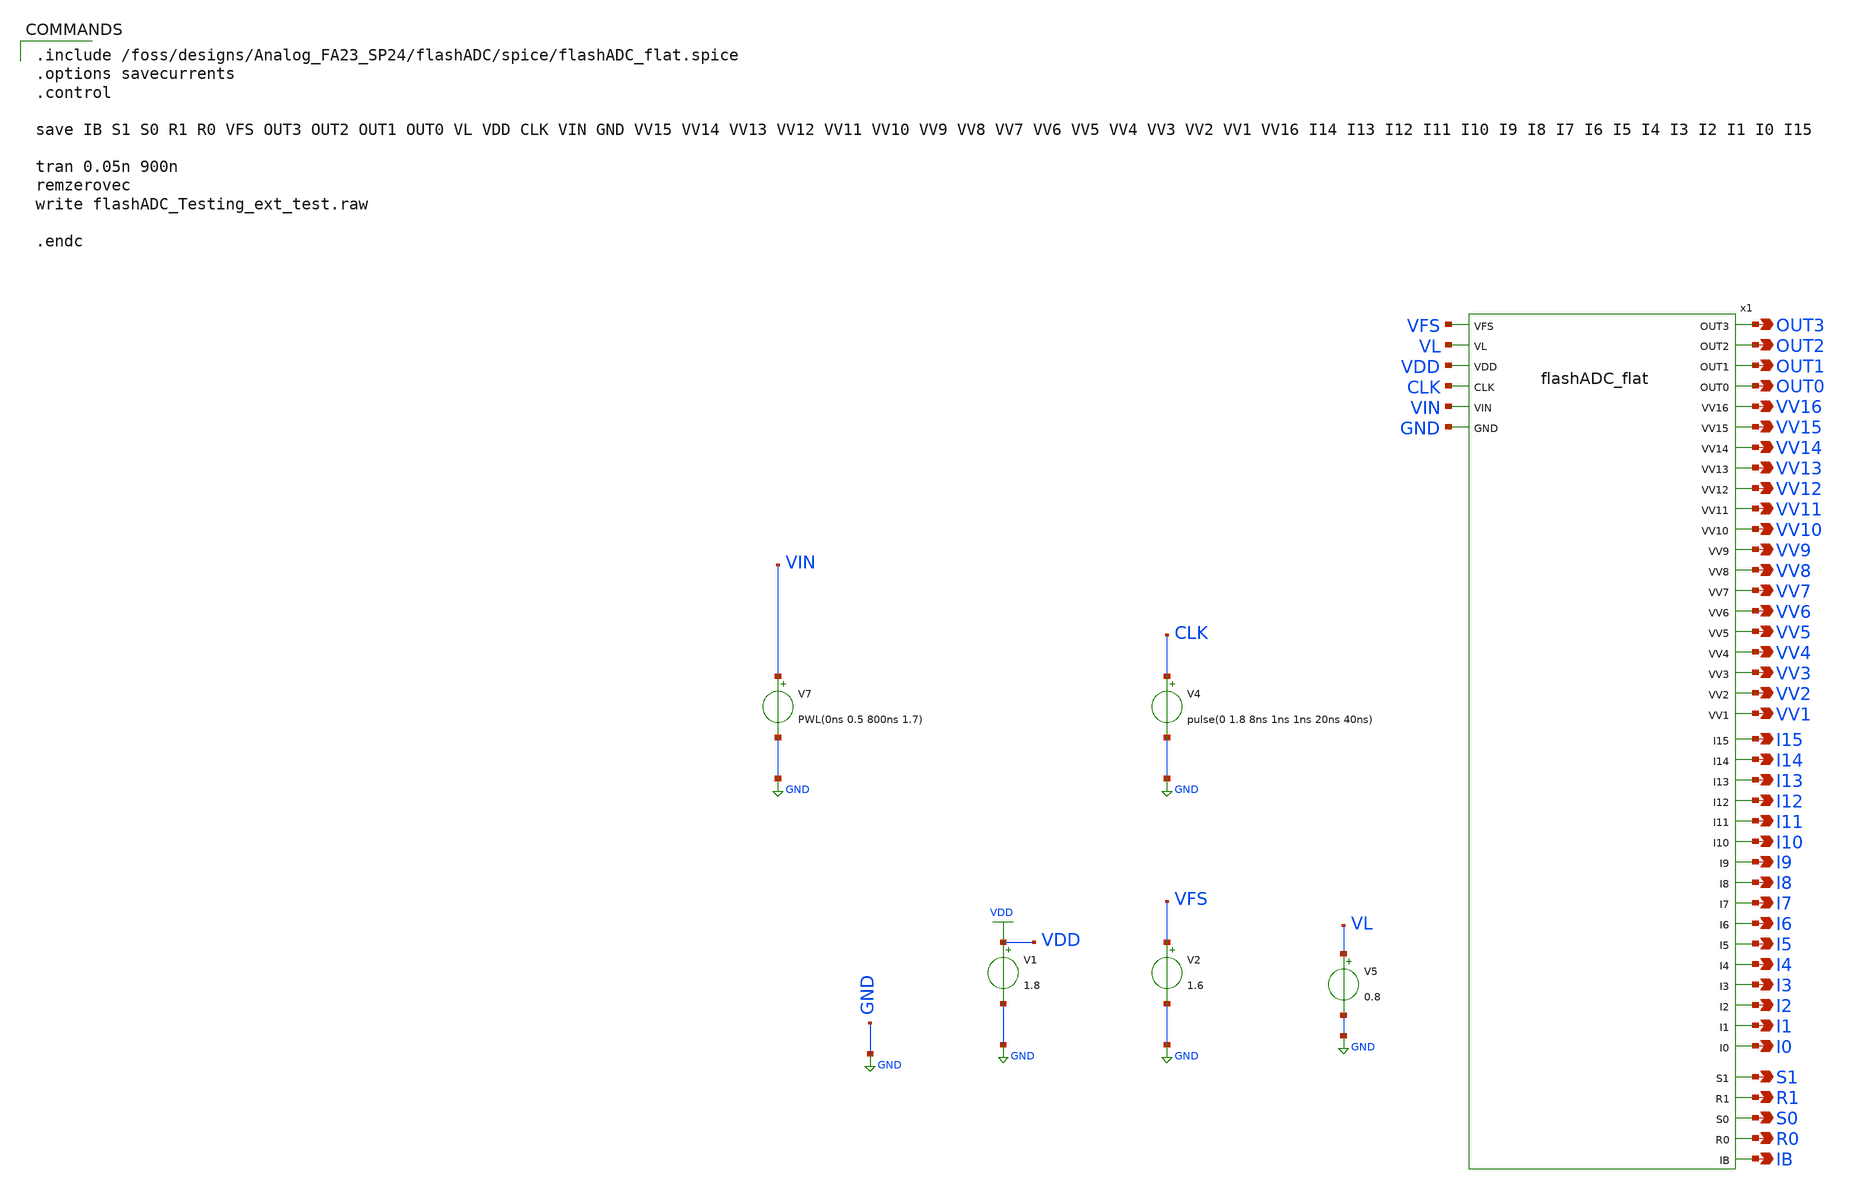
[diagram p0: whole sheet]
** sch_path: flashADC/xschem/flashADC_Testing_ext.sch
.lib $::SKYWATER_MODELS/sky130.lib.spice tt
.include $::SKYWATER_STDCELLS/sky130_fd_sc_hd.spice

**.subckt flashADC_Testing_ext OUT3 OUT2 OUT1 OUT0 VV16 VV15 VV14 VV13 VV12 VV11 VV10 VV9 VV8 VV7
*+ VV6 VV5 VV4 VV3 VV2 VV1 I15 I14 I13 I12 I11 I10 I9 I8 I7 I6 I5 I4 I3 I2 I1 I0 S1 R1 S0 R0 IB
*.opin OUT3
*.opin OUT2
*.opin OUT1
*.opin OUT0
*.opin VV16
*.opin VV15
*.opin VV14
*.opin VV13
*.opin VV12
*.opin VV11
*.opin VV10
*.opin VV9
*.opin VV8
*.opin VV7
*.opin VV6
*.opin VV5
*.opin VV4
*.opin VV3
*.opin VV2
*.opin VV1
*.opin I15
*.opin I14
*.opin I13
*.opin I12
*.opin I11
*.opin I10
*.opin I9
*.opin I8
*.opin I7
*.opin I6
*.opin I5
*.opin I4
*.opin I3
*.opin I2
*.opin I1
*.opin I0
*.opin S1
*.opin R1
*.opin S0
*.opin R0
*.opin IB
V4 CLK GND pulse(0 1.8 8ns 1ns 1ns 20ns 40ns)
V1 VDD GND 1.8
V2 VFS GND 1.6
V5 VL GND 0.8
V7 VIN GND PWL(0ns 0.5 800ns 1.7)
x1 VFS OUT3 OUT2 OUT1 OUT0 VL VDD CLK VIN GND VV15 VV14 VV13 VV12 VV11 VV10 VV9 VV8 VV7 VV6 VV5 VV4
+ VV3 VV2 VV1 VV16 I14 I13 I12 I11 I10 I9 I8 I7 I6 I5 I4 I3 I2 I1 I0 I15 S1 R1 S0 R0 IB flashADC_flat
**** begin user architecture code

.include /foss/designs/Analog_FA23_SP24/flashADC/spice/flashADC_flat.spice
.options savecurrents
.control

save IB S1 S0 R1 R0 VFS OUT3 OUT2 OUT1 OUT0 VL VDD CLK VIN GND VV15 VV14 VV13 VV12 VV11 VV10 VV9 VV8
+ VV7 VV6 VV5 VV4 VV3 VV2 VV1 VV16 I14 I13 I12 I11 I10 I9 I8 I7 I6 I5 I4 I3 I2 I1 I0 I15

tran 0.05n 900n
remzerovec
write flashADC_Testing_ext_test.raw

.endc


**** end user architecture code
**.ends
.GLOBAL GND
.GLOBAL VDD
.end
